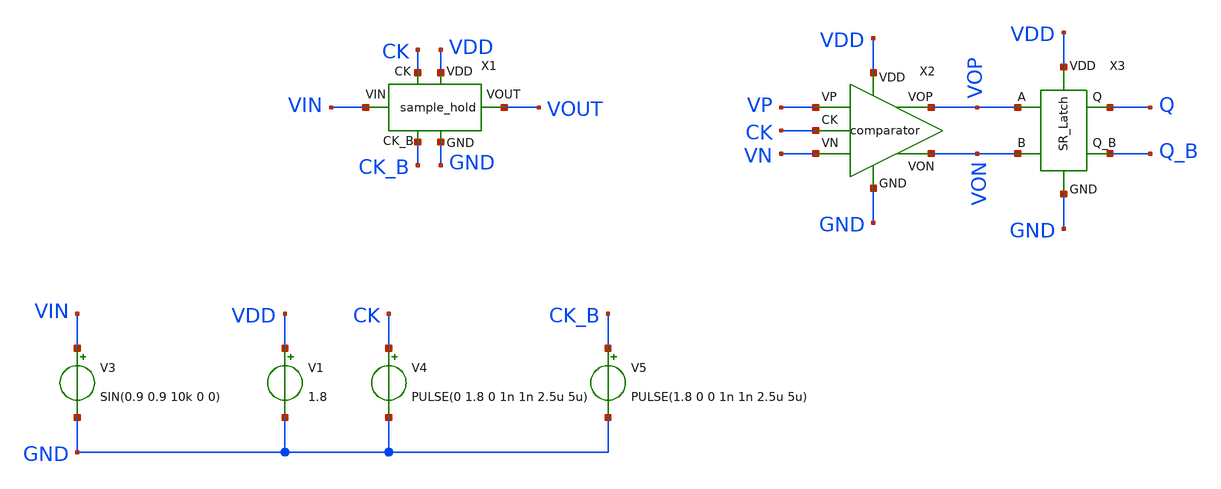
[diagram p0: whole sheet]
** sch_path: xschem/adc_top.sch
**.subckt adc_top
X1 GND VDD VIN VOUT CK CK_B sample_hold
X2 VP VN GND VON VOP VDD CK comparator
X3 VOP VON GND VDD Q Q_B SR_Latch
V1 VDD GND 1.8
V3 VIN GND SIN(0.9 0.9 10k 0 0)
V4 CK GND PULSE(0 1.8 0 1n 1n 2.5u 5u)
V5 CK_B GND PULSE(1.8 0 0 1n 1n 2.5u 5u)
**.ends
.end
